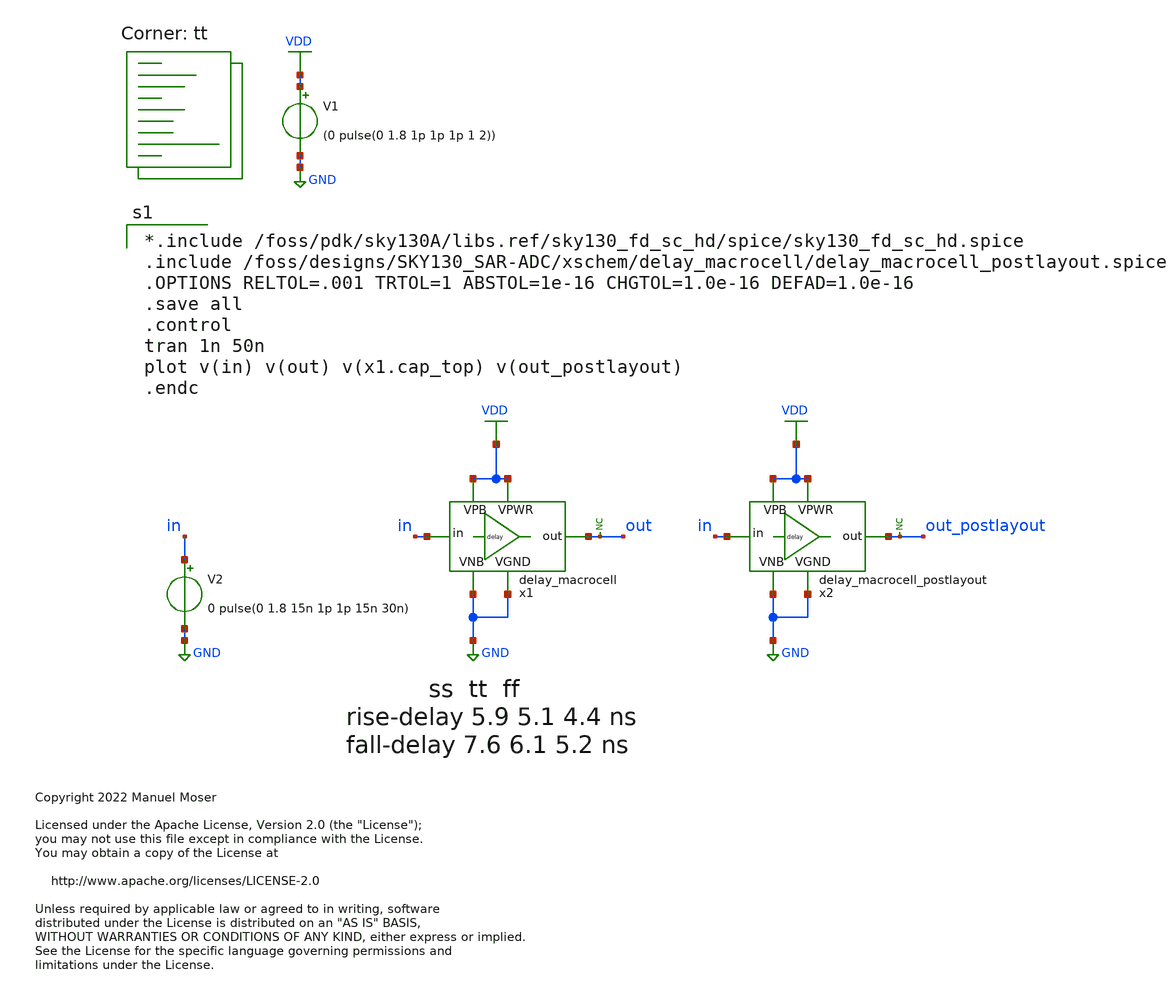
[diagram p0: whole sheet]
** sch_path: xschem/archive/adc_delay_macrocell/delay_macrocell_tb.sch
* Copyright 2022 Manuel Moser
* Licensed under the Apache License, Version 2.0 (the "License");
**.subckt delay_macrocell_tb
V1 VDD GND (0 pulse(0 1.8 1p 1p 1p 1 2))
V2 in GND 0 pulse(0 1.8 15n 1p 1p 15n 30n)
x1 VDD in out GND GND VDD delay_macrocell
* noconn out
* noconn out_postlayout
x2 VDD in out_postlayout GND VDD GND delay_macrocell_postlayout
**** begin user architecture code

*.include /foss/pdk/sky130A/libs.ref/sky130_fd_sc_hd/spice/sky130_fd_sc_hd.spice
.include /foss/designs/SKY130_SAR-ADC/xschem/delay_macrocell/delay_macrocell_postlayout.spice
.OPTIONS RELTOL=.001 TRTOL=1 ABSTOL=1e-16 CHGTOL=1.0e-16 DEFAD=1.0e-16
.save all
.control
tran 1n 50n
plot v(in) v(out) v(x1.cap_top) v(out_postlayout)
.endc

.lib $::SKYWATER_MODELS/sky130.lib.spice tt
**** end user architecture code
**.ends

* expanding   symbol:  delay_macrocell.sym # of pins=6
** sym_path: xschem/delay_macrocell/delay_macrocell.sym
** sch_path: xschem/delay_macrocell/delay_macrocell.sch
.subckt delay_macrocell VPWR in out VGND VNB VPB
*.iopin VPWR
*.iopin VGND
*.ipin in
*.opin out
*.iopin VPB
*.iopin VNB
XM2 cap_top in VGND VNB sky130_fd_pr__nfet_01v8 L=4 W=0.42 nf=1 ad='int((nf+1)/2) * W/nf * 0.29' as='int((nf+2)/2) * W/nf * 0.29'
+ pd='2*int((nf+1)/2) * (W/nf + 0.29)' ps='2*int((nf+2)/2) * (W/nf + 0.29)' nrd='0.29 / W' nrs='0.29 / W'
+ sa=0 sb=0 sd=0 mult=1 m=1
XM3 net2 cap_top VGND VNB sky130_fd_pr__nfet_01v8 L=0.15 W=0.42 nf=1 ad='int((nf+1)/2) * W/nf * 0.29'
+ as='int((nf+2)/2) * W/nf * 0.29' pd='2*int((nf+1)/2) * (W/nf + 0.29)' ps='2*int((nf+2)/2) * (W/nf + 0.29)'
+ nrd='0.29 / W' nrs='0.29 / W' sa=0 sb=0 sd=0 mult=1 m=1
XM4 out cap_top net2 VNB sky130_fd_pr__nfet_01v8 L=0.15 W=0.42 nf=1 ad='int((nf+1)/2) * W/nf * 0.29'
+ as='int((nf+2)/2) * W/nf * 0.29' pd='2*int((nf+1)/2) * (W/nf + 0.29)' ps='2*int((nf+2)/2) * (W/nf + 0.29)'
+ nrd='0.29 / W' nrs='0.29 / W' sa=0 sb=0 sd=0 mult=1 m=1
XM5 out cap_top net1 VPB sky130_fd_pr__pfet_01v8 L=0.15 W=0.84 nf=1 ad='int((nf+1)/2) * W/nf * 0.29'
+ as='int((nf+2)/2) * W/nf * 0.29' pd='2*int((nf+1)/2) * (W/nf + 0.29)' ps='2*int((nf+2)/2) * (W/nf + 0.29)'
+ nrd='0.29 / W' nrs='0.29 / W' sa=0 sb=0 sd=0 mult=1 m=1
XM6 net1 cap_top VPWR VPB sky130_fd_pr__pfet_01v8 L=0.15 W=0.84 nf=1 ad='int((nf+1)/2) * W/nf * 0.29'
+ as='int((nf+2)/2) * W/nf * 0.29' pd='2*int((nf+1)/2) * (W/nf + 0.29)' ps='2*int((nf+2)/2) * (W/nf + 0.29)'
+ nrd='0.29 / W' nrs='0.29 / W' sa=0 sb=0 sd=0 mult=1 m=1
XM7 VPWR out net2 VNB sky130_fd_pr__nfet_01v8 L=0.15 W=0.84 nf=2 ad='int((nf+1)/2) * W/nf * 0.29' as='int((nf+2)/2) * W/nf * 0.29'
+ pd='2*int((nf+1)/2) * (W/nf + 0.29)' ps='2*int((nf+2)/2) * (W/nf + 0.29)' nrd='0.29 / W' nrs='0.29 / W'
+ sa=0 sb=0 sd=0 mult=1 m=1
XM8 VGND out net1 VPB sky130_fd_pr__pfet_01v8 L=0.15 W=1.68 nf=2 ad='int((nf+1)/2) * W/nf * 0.29' as='int((nf+2)/2) * W/nf * 0.29'
+ pd='2*int((nf+1)/2) * (W/nf + 0.29)' ps='2*int((nf+2)/2) * (W/nf + 0.29)' nrd='0.29 / W' nrs='0.29 / W'
+ sa=0 sb=0 sd=0 mult=1 m=1
XC1 cap_top VGND sky130_fd_pr__cap_mim_m3_1 W=3.68 L=1.93 MF=1 m=1
XC2 cap_top VGND sky130_fd_pr__cap_mim_m3_1 W=2.63 L=1.93 MF=1 m=1
XM9 cap_top in VPWR VPB sky130_fd_pr__pfet_01v8_lvt L=4 W=0.84 nf=1 ad='int((nf+1)/2) * W/nf * 0.29'
+ as='int((nf+2)/2) * W/nf * 0.29' pd='2*int((nf+1)/2) * (W/nf + 0.29)' ps='2*int((nf+2)/2) * (W/nf + 0.29)'
+ nrd='0.29 / W' nrs='0.29 / W' sa=0 sb=0 sd=0 mult=1 m=1
.ends

.GLOBAL VDD
.GLOBAL GND
.end
